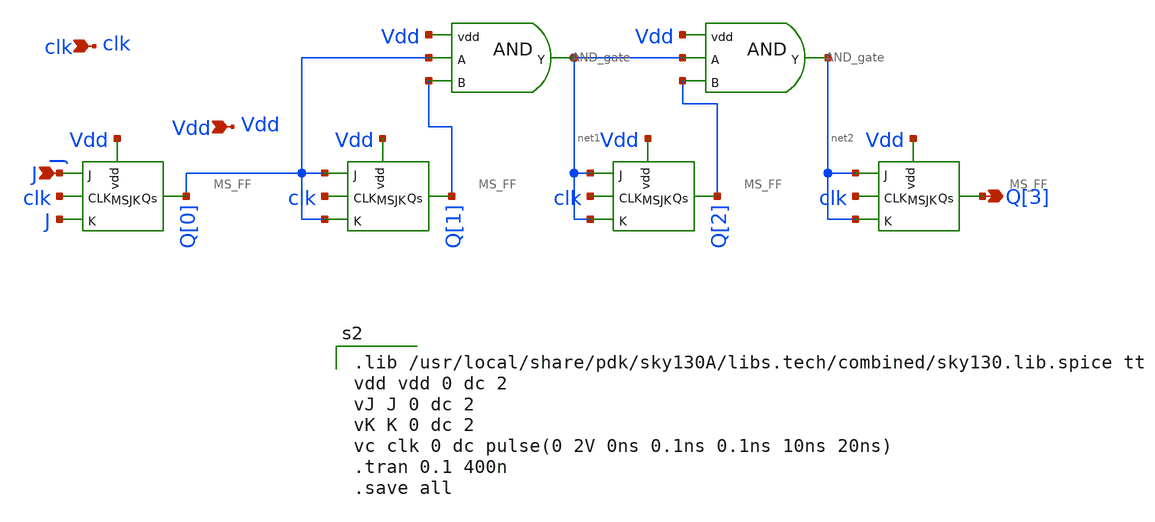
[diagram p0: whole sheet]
** sch_path: Circuit Files/circuits/circuits/syncount.sch
**.subckt syncount Vdd Q[3] clk J
*.ipin Vdd
*.opin Q[3]
*.ipin clk
*.ipin J
x5 Vdd J Q[0] clk J MS_FF
x1 Vdd Q[0] Q[1] clk Q[0] MS_FF
x2 Vdd net1 Q[2] clk net1 MS_FF
x3 Vdd net2 Q[3] clk net2 MS_FF
x4 Vdd Q[0] net1 Q[1] AND_gate
x6 Vdd net1 net2 Q[2] AND_gate
**** begin user architecture code

.lib /usr/local/share/pdk/sky130A/libs.tech/combined/sky130.lib.spice tt
vdd vdd 0 dc 2
vJ J 0 dc 2
vK K 0 dc 2
vc clk 0 dc pulse(0 2V 0ns 0.1ns 0.1ns 10ns 20ns)
.tran 0.1 400n
.save all


**** end user architecture code
**.ends

* expanding   symbol:  daVLSI_World/circuits/MS_FF.sym # of pins=5
** sym_path: Circuit Files/circuits/circuits/MS_FF.sym
** sch_path: Circuit Files/circuits/circuits/MS_FF.sch
.subckt MS_FF vdd J Qs CLK K
*.ipin J
*.ipin vdd
*.ipin CLK
*.ipin K
*.opin Qs
x3 vdd Qm net3 net1 GND NAND_gate
x5 vdd net1 Qm net4 GND NAND_gate
x2 vdd net3 net2 J CLK 3_NAND_GATE
x6 vdd net4 CLK K Qs 3_NAND_GATE
x1 vdd Qs net6 net2 GND NAND_gate
x4 vdd net2 Qs net7 GND NAND_gate
x7 vdd net6 Qm Qm net5 3_NAND_GATE
x8 vdd net7 net5 net1 net1 3_NAND_GATE
x9 net8 net9 net10 inverter_vtc
**** begin user architecture code

.IC v(Qs)=0

**** end user architecture code
.ends


* expanding   symbol:  daVLSI_World/gates/AND_gate.sym # of pins=4
** sym_path: Circuit Files/Logic gate design using MOSFETS/gates/AND_gate.sym
** sch_path: Circuit Files/Logic gate design using MOSFETS/gates/AND_gate.sch
.subckt AND_gate vdd A Y B
*.opin Y
*.ipin A
*.ipin B
*.ipin vdd
x1 vdd net1 A B GND NAND_gate
x2 vdd net1 Y inverter_vtc
.ends


* expanding   symbol:  daVLSI_World/gates/NAND_gate.sym # of pins=5
** sym_path: Circuit Files/Logic gate design using MOSFETS/gates/NAND_gate.sym
** sch_path: Circuit Files/Logic gate design using MOSFETS/gates/NAND_gate.sch
.subckt NAND_gate vdd Y A B gnd
*.ipin A
*.ipin B
*.opin Y
*.ipin vdd
*.ipin gnd
XM1 Y A net1 gnd sky130_fd_pr__nfet_01v8 L=0.15 W=1 nf=1 ad='int((nf+1)/2) * W/nf * 0.29' as='int((nf+2)/2) * W/nf * 0.29'
+ pd='2*int((nf+1)/2) * (W/nf + 0.29)' ps='2*int((nf+2)/2) * (W/nf + 0.29)' nrd='0.29 / W' nrs='0.29 / W'
+ sa=0 sb=0 sd=0 mult=1 m=1
XM2 net1 B gnd gnd sky130_fd_pr__nfet_01v8 L=0.15 W=1 nf=1 ad='int((nf+1)/2) * W/nf * 0.29' as='int((nf+2)/2) * W/nf * 0.29'
+ pd='2*int((nf+1)/2) * (W/nf + 0.29)' ps='2*int((nf+2)/2) * (W/nf + 0.29)' nrd='0.29 / W' nrs='0.29 / W'
+ sa=0 sb=0 sd=0 mult=1 m=1
XM3 Y A vdd vdd sky130_fd_pr__pfet_01v8 L=0.15 W=2 nf=1 ad='int((nf+1)/2) * W/nf * 0.29' as='int((nf+2)/2) * W/nf * 0.29'
+ pd='2*int((nf+1)/2) * (W/nf + 0.29)' ps='2*int((nf+2)/2) * (W/nf + 0.29)' nrd='0.29 / W' nrs='0.29 / W'
+ sa=0 sb=0 sd=0 mult=1 m=1
XM4 Y B vdd vdd sky130_fd_pr__pfet_01v8 L=0.15 W=2 nf=1 ad='int((nf+1)/2) * W/nf * 0.29' as='int((nf+2)/2) * W/nf * 0.29'
+ pd='2*int((nf+1)/2) * (W/nf + 0.29)' ps='2*int((nf+2)/2) * (W/nf + 0.29)' nrd='0.29 / W' nrs='0.29 / W'
+ sa=0 sb=0 sd=0 mult=1 m=1
.ends


* expanding   symbol:  daVLSI_World/gates/3_NAND_GATE.sym # of pins=5
** sym_path: Circuit Files/Logic gate design using MOSFETS/gates/3_NAND_GATE.sym
** sch_path: Circuit Files/Logic gate design using MOSFETS/gates/3_NAND_GATE.sch
.subckt 3_NAND_GATE vdd Y A B C
*.ipin A
*.ipin B
*.opin Y
*.ipin vdd
*.ipin C
XM1 Y A net1 GND sky130_fd_pr__nfet_01v8 L=0.15 W=1 nf=1 ad='int((nf+1)/2) * W/nf * 0.29' as='int((nf+2)/2) * W/nf * 0.29'
+ pd='2*int((nf+1)/2) * (W/nf + 0.29)' ps='2*int((nf+2)/2) * (W/nf + 0.29)' nrd='0.29 / W' nrs='0.29 / W'
+ sa=0 sb=0 sd=0 mult=1 m=1
XM2 net1 B net2 GND sky130_fd_pr__nfet_01v8 L=0.15 W=1 nf=1 ad='int((nf+1)/2) * W/nf * 0.29' as='int((nf+2)/2) * W/nf * 0.29'
+ pd='2*int((nf+1)/2) * (W/nf + 0.29)' ps='2*int((nf+2)/2) * (W/nf + 0.29)' nrd='0.29 / W' nrs='0.29 / W'
+ sa=0 sb=0 sd=0 mult=1 m=1
XM3 Y A vdd vdd sky130_fd_pr__pfet_01v8 L=0.15 W=2 nf=1 ad='int((nf+1)/2) * W/nf * 0.29' as='int((nf+2)/2) * W/nf * 0.29'
+ pd='2*int((nf+1)/2) * (W/nf + 0.29)' ps='2*int((nf+2)/2) * (W/nf + 0.29)' nrd='0.29 / W' nrs='0.29 / W'
+ sa=0 sb=0 sd=0 mult=1 m=1
XM4 Y B vdd vdd sky130_fd_pr__pfet_01v8 L=0.15 W=2 nf=1 ad='int((nf+1)/2) * W/nf * 0.29' as='int((nf+2)/2) * W/nf * 0.29'
+ pd='2*int((nf+1)/2) * (W/nf + 0.29)' ps='2*int((nf+2)/2) * (W/nf + 0.29)' nrd='0.29 / W' nrs='0.29 / W'
+ sa=0 sb=0 sd=0 mult=1 m=1
XM5 net2 C GND GND sky130_fd_pr__nfet_01v8 L=0.15 W=1 nf=1 ad='int((nf+1)/2) * W/nf * 0.29' as='int((nf+2)/2) * W/nf * 0.29'
+ pd='2*int((nf+1)/2) * (W/nf + 0.29)' ps='2*int((nf+2)/2) * (W/nf + 0.29)' nrd='0.29 / W' nrs='0.29 / W'
+ sa=0 sb=0 sd=0 mult=1 m=1
XM6 Y C vdd vdd sky130_fd_pr__pfet_01v8 L=0.15 W=2 nf=1 ad='int((nf+1)/2) * W/nf * 0.29' as='int((nf+2)/2) * W/nf * 0.29'
+ pd='2*int((nf+1)/2) * (W/nf + 0.29)' ps='2*int((nf+2)/2) * (W/nf + 0.29)' nrd='0.29 / W' nrs='0.29 / W'
+ sa=0 sb=0 sd=0 mult=1 m=1
.ends


* expanding   symbol:  daVLSI_World/gates/inverter_vtc.sym # of pins=3
** sym_path: Circuit Files/Logic gate design using MOSFETS/gates/inverter_vtc.sym
** sch_path: Circuit Files/Logic gate design using MOSFETS/gates/inverter_vtc.sch
.subckt inverter_vtc vdd vin vout
*.ipin vin
*.opin vout
*.ipin vdd
XM1 vout vin GND GND sky130_fd_pr__nfet_01v8 L=0.15 W=1 nf=1 ad='int((nf+1)/2) * W/nf * 0.29' as='int((nf+2)/2) * W/nf * 0.29'
+ pd='2*int((nf+1)/2) * (W/nf + 0.29)' ps='2*int((nf+2)/2) * (W/nf + 0.29)' nrd='0.29 / W' nrs='0.29 / W'
+ sa=0 sb=0 sd=0 mult=1 m=1
XM2 vout vin vdd vdd sky130_fd_pr__pfet_01v8 L=0.15 W=2 nf=1 ad='int((nf+1)/2) * W/nf * 0.29' as='int((nf+2)/2) * W/nf * 0.29'
+ pd='2*int((nf+1)/2) * (W/nf + 0.29)' ps='2*int((nf+2)/2) * (W/nf + 0.29)' nrd='0.29 / W' nrs='0.29 / W'
+ sa=0 sb=0 sd=0 mult=1 m=1
.ends

.GLOBAL GND
.end
